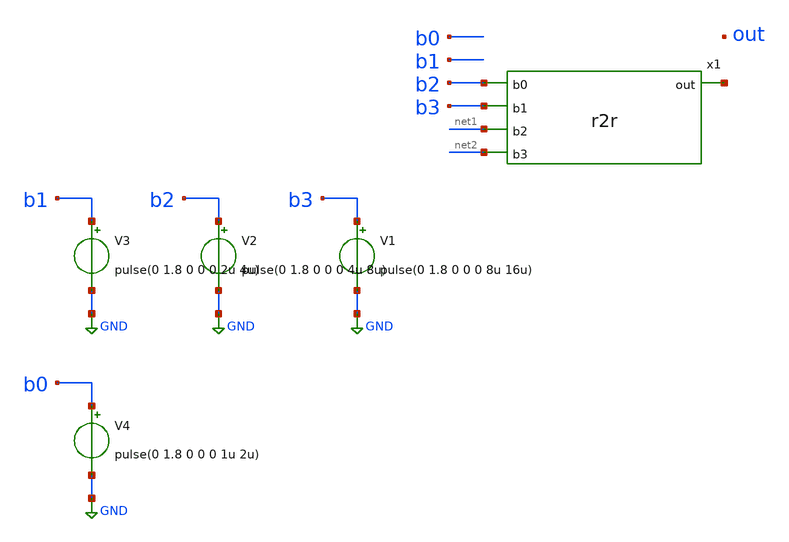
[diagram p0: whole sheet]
** sch_path: xschem/testbench.sch
**.subckt testbench
x1 b2 b3 net1 net2 net3 r2r
V1 b3 GND pulse(0 1.8 0 0 0 8u 16u)
V2 b2 GND pulse(0 1.8 0 0 0 4u 8u)
V3 b1 GND pulse(0 1.8 0 0 0 2u 4u)
V4 b0 GND pulse(0 1.8 0 0 0 1u 2u)
**** begin user architecture code


.lib /home/matt/work/asic-workshop/shuttle-2404/pdk/sky130A/libs.tech/ngspice/sky130.lib.spice tt
.tran 1n 20u uic
.save all


**** end user architecture code
**.ends

* expanding   symbol:  r2r.sym # of pins=5
** sym_path: xschem/r2r.sym
** sch_path: xschem/r2r.sch
.subckt r2r b0 b1 b2 b3 out
*.ipin b1
*.opin out
*.ipin b0
*.ipin b2
*.ipin b3
R1 b0 net1 1k m=1
R2 b1 net2 1k m=1
R3 b2 net3 1k m=1
R4 net1 GND 1k m=1
R5 b3 out 1k m=1
R6 net2 net1 500 m=1
R7 net3 net2 500 m=1
R8 out net3 500 m=1
.ends

.GLOBAL GND
.end
